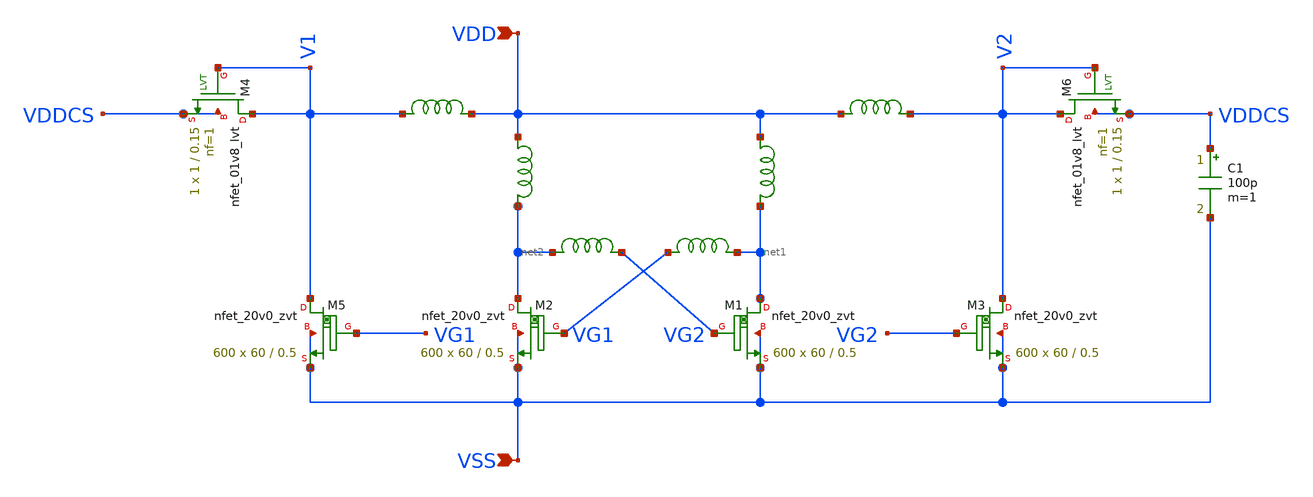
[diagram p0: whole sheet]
** sch_path: design/LELO_SVOD_SKY130A/LELO_EXSC.sch
**.subckt LELO_EXSC VSS VDD
*.ipin VSS
*.ipin VDD
x3 VDD net1 1812PS-102_imp
x4 VDD net2 1812PS-102_imp
XM1 net1 VG2 VSS VSS sky130_fd_pr__nfet_20v0_zvt W=60 L=0.5 m=600
XM2 net2 VG1 VSS VSS sky130_fd_pr__nfet_20v0_zvt W=60 L=0.5 m=600
x1 net2 VG2 1812PS-104_imp
x2 VG1 net1 1812PS-104_imp
XM3 V2 VG2 VSS VSS sky130_fd_pr__nfet_20v0_zvt W=60 L=0.5 m=600
C1 VDDCS VSS 100p m=1
XM5 V1 VG1 VSS VSS sky130_fd_pr__nfet_20v0_zvt W=60 L=0.5 m=600
x5 VDD V2 1812PS-104_imp
x6 V1 VDD 1812PS-104_imp
XM4 V1 V1 VDDCS VDDCS sky130_fd_pr__nfet_01v8_lvt L=0.15 W=1 nf=1 ad='int((1 + 1)/2) * 1 / 1 * 0.29'
+ as='int((1 + 2)/2) * 1 / 1 * 0.29' pd='2*int((1 + 1)/2) * (1 / 1 + 0.29)' ps='2*int((1 + 2)/2) * (1 / 1 + 0.29)'
+ nrd='0.29 / 1 ' nrs='0.29 / 1 ' sa=0 sb=0 sd=0 mult=1 m=1
XM6 V2 V2 VDDCS VDDCS sky130_fd_pr__nfet_01v8_lvt L=0.15 W=1 nf=1 ad='int((1 + 1)/2) * 1 / 1 * 0.29'
+ as='int((1 + 2)/2) * 1 / 1 * 0.29' pd='2*int((1 + 1)/2) * (1 / 1 + 0.29)' ps='2*int((1 + 2)/2) * (1 / 1 + 0.29)'
+ nrd='0.29 / 1 ' nrs='0.29 / 1 ' sa=0 sb=0 sd=0 mult=1 m=1
**.ends

* expanding   symbol:  LELO_SVOD_SKY130A/1812PS-102_imp.sym # of pins=2
** sym_path: design/LELO_SVOD_SKY130A/1812PS-102_imp.sym

.subckt 1812PS-102_imp port1 port2
X1 port1 port2 Model1D R1=60 R2=0.054 C= 0.15p K1=0.000001 K2=0.064 K3= 1u K4=1E-06 K5=0.000001 L=0
+ Is=0 a=0 L_Z0=0 L_EL=0 L_F0=0E6 PkZ=1282.46492
.ends 1812PS-102_imp

* expanding   symbol:  LELO_SVOD_SKY130A/1812PS-104_imp.sym # of pins=2
** sym_path: design/LELO_SVOD_SKY130A/1812PS-104_imp.sym

.subckt 1812PS-104_imp port1 port2
X1 port1 port2 Model1D R1=40 R2=1.3 C= 1.6p K1=0.000001 K2=13.98 K3= 100u K4=0.000001 K5=0.000001
+ L=0 Is=0 a=0 L_Z0=0 L_EL=0 L_F0=0E6 PkZ=48065.0165
.ends 1812PS-104_imp
.end
